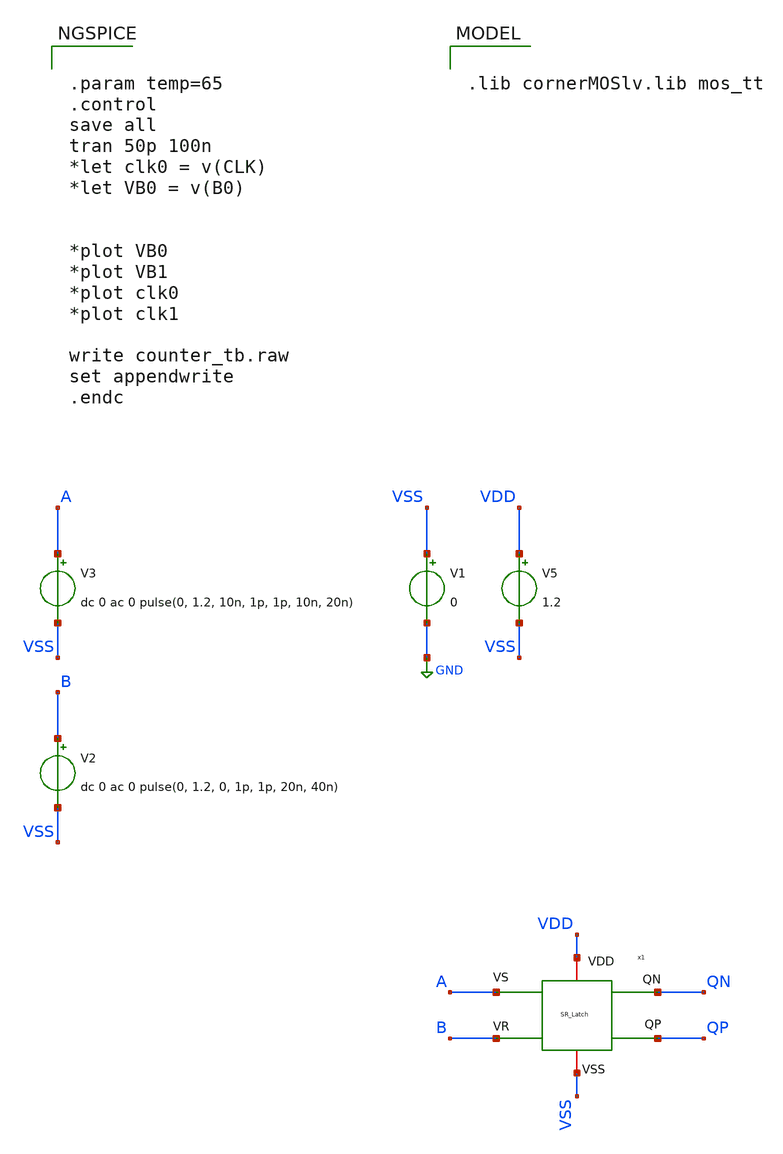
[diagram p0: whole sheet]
** sch_path: GROTDC_SIM/tb_SR_Latch.sch
**.subckt tb_SR_Latch
V1 VSS GND 0
V3 A VSS dc 0 ac 0 pulse(0, 1.2, 10n, 1p, 1p, 10n, 20n)
V5 VDD VSS 1.2
V2 B VSS dc 0 ac 0 pulse(0, 1.2, 0, 1p, 1p, 20n, 40n)
x1 VDD A QN QP B VSS SR_Latch
**** begin user architecture code


.param temp=65
.control
save all
tran 50p 100n
*let clk0 = v(CLK)
*let VB0 = v(B0)


*plot VB0
*plot VB1
*plot clk0
*plot clk1

write counter_tb.raw
set appendwrite
.endc



.lib cornerMOSlv.lib mos_tt

**** end user architecture code
**.ends
.GLOBAL GND
.end
